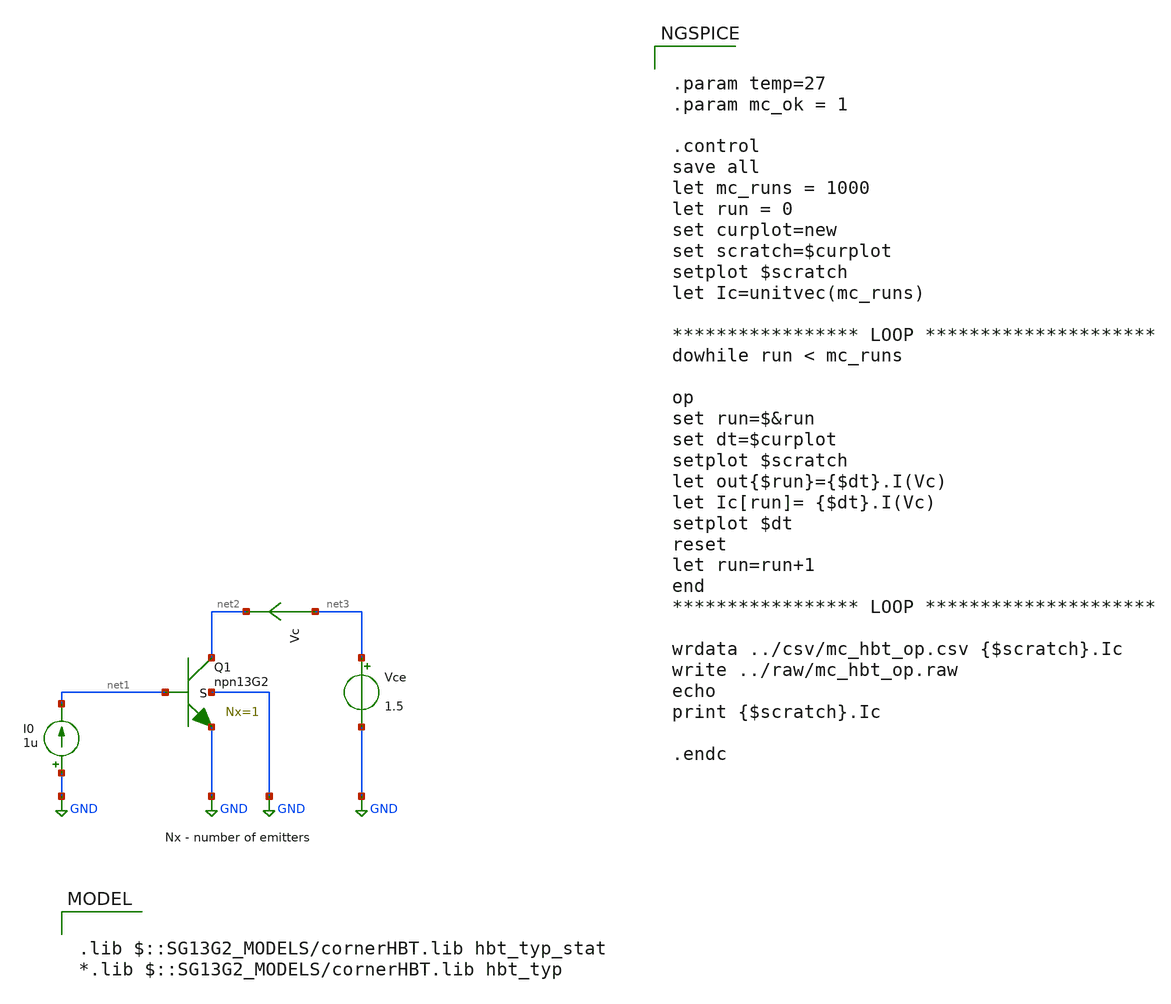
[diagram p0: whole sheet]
** sch_path: ihp-sg13g2/libs.tech/xschem/sg13g2_tests/mc_hbt_13g2.sch
* Copyright 2023 IHP PDK Authors
**.subckt mc_hbt_13g2
Vce net3 GND 1.5
I0 GND net1 1u
XQ1 net2 net1 GND GND npn13G2 Nx=1 mm_ok=1
Vc net3 net2 0
.save i(vc)
**** begin user architecture code

.lib $::SG13G2_MODELS/cornerHBT.lib hbt_typ_stat
*.lib $::SG13G2_MODELS/cornerHBT.lib hbt_typ



.param temp=27
.param mc_ok = 1

.control
save all
let mc_runs = 1000
let run = 0
set curplot=new
set scratch=$curplot
setplot $scratch
let Ic=unitvec(mc_runs)

***************** LOOP *********************
dowhile run < mc_runs

op
set run=$&run
set dt=$curplot
setplot $scratch
let out{$run}={$dt}.I(Vc)
let Ic[run]= {$dt}.I(Vc)
setplot $dt
reset
let run=run+1
end
***************** LOOP *********************

wrdata ../csv/mc_hbt_op.csv {$scratch}.Ic
write ../raw/mc_hbt_op.raw
echo
print {$scratch}.Ic

.endc


**** end user architecture code
**.ends
.GLOBAL GND
.end
